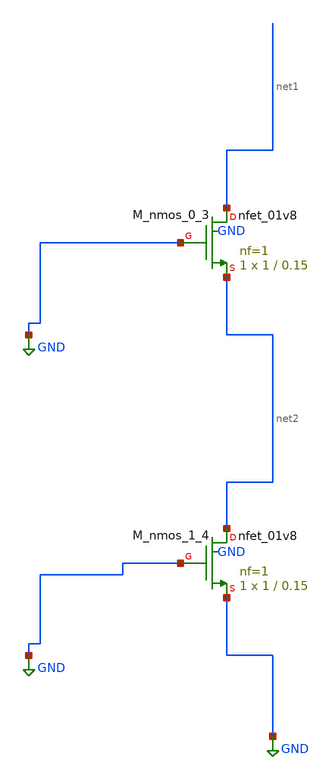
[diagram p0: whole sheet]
** sch_path: schematics/AMSNet/132.sch
**.subckt 132
XM_nmos_0_3 net1 GND net2 GND sky130_fd_pr__nfet_01v8 L=0.15 W=1 nf=1 ad='int((1 + 1)/2) * 1 / 1 * 0.29'
+ as='int((1 + 2)/2) * 1 / 1 * 0.29' pd='2*int((1 + 1)/2) * (1 / 1 + 0.29)' ps='2*int((1 + 2)/2) * (1 / 1 + 0.29)'
+ nrd='0.29 / 1 ' nrs='0.29 / 1 ' sa=0 sb=0 sd=0 mult=1 m=1
XM_nmos_1_4 net2 GND GND GND sky130_fd_pr__nfet_01v8 L=0.15 W=1 nf=1 ad='int((1 + 1)/2) * 1 / 1 * 0.29'
+ as='int((1 + 2)/2) * 1 / 1 * 0.29' pd='2*int((1 + 1)/2) * (1 / 1 + 0.29)' ps='2*int((1 + 2)/2) * (1 / 1 + 0.29)'
+ nrd='0.29 / 1 ' nrs='0.29 / 1 ' sa=0 sb=0 sd=0 mult=1 m=1
**.ends
.GLOBAL GND
.end
